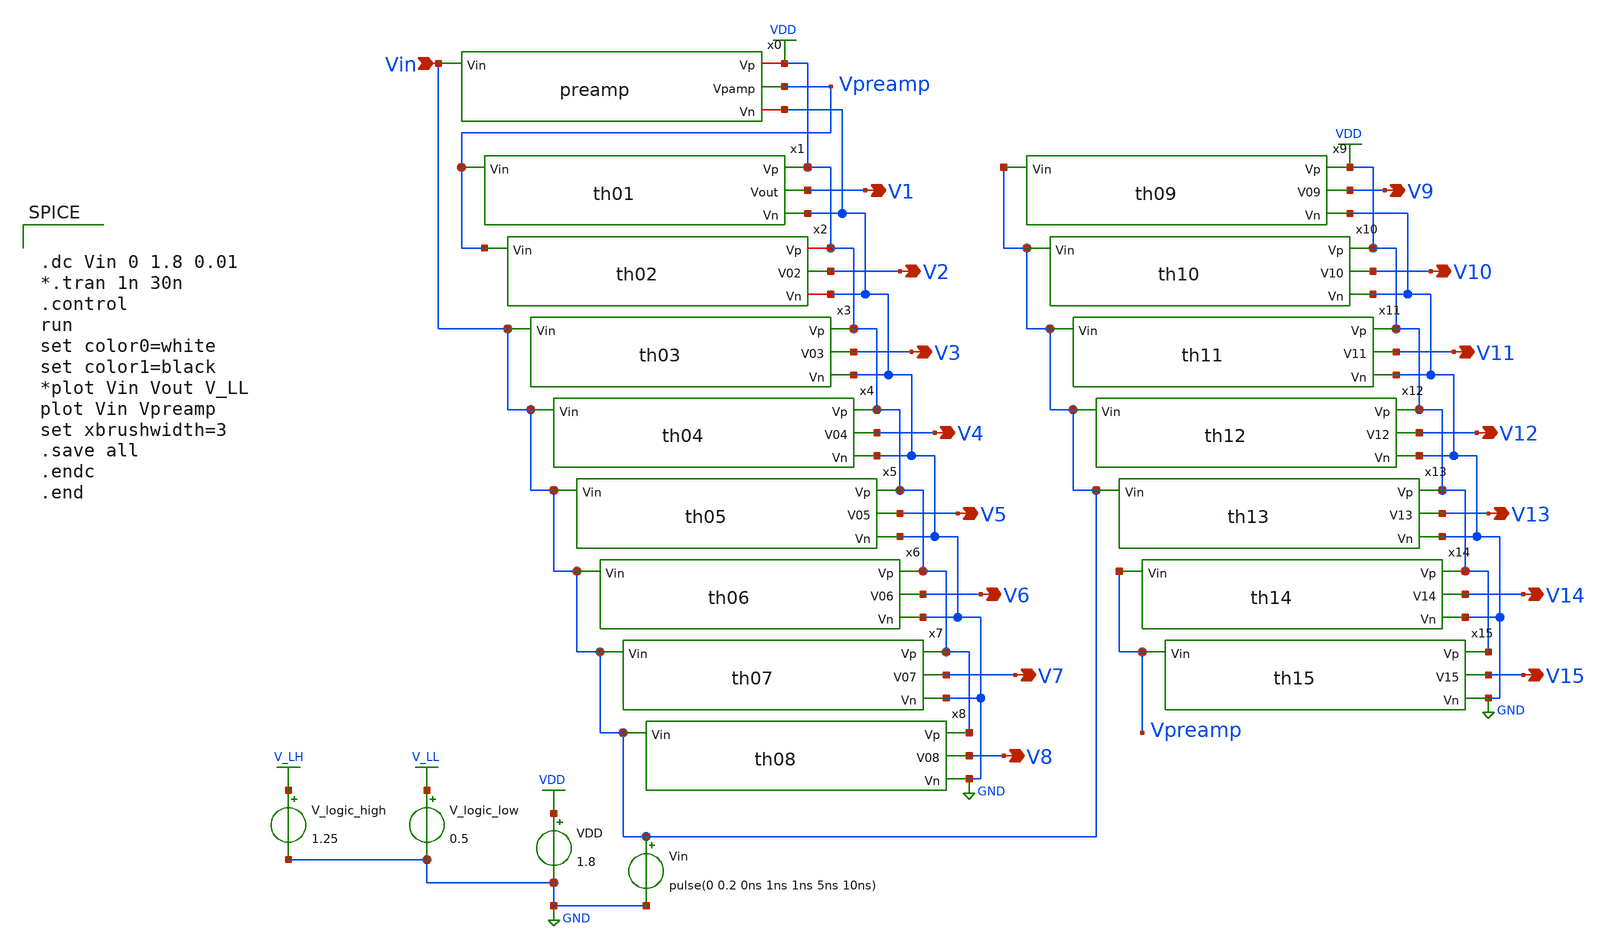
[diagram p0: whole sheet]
** sch_path: xschem/Vth_sch/Pre_layout/Analog_With_Sub.sch
**.subckt Analog_With_Sub V1 Vin V2 V3 V4 V5 V6 V7 V8 V9 V10 V11 V12 V13 V14 V15
*.opin V1
*.ipin Vin
*.opin V2
*.opin V3
*.opin V4
*.opin V5
*.opin V6
*.opin V7
*.opin V8
*.opin V9
*.opin V10
*.opin V11
*.opin V12
*.opin V13
*.opin V14
*.opin V15
VDD VDD GND 1.8
Vin Vin GND pulse(0 0.2 0ns 1ns 1ns 5ns 10ns)
V_logic_high V_LH GND 1.25
V_logic_low V_LL GND 0.5
x0 VDD Vin Vpreamp GND preamp
x1 VDD Vpreamp V1 GND th01
x2 VDD Vpreamp V2 GND th02
x3 VDD V3 Vin GND th03
x4 VDD V4 Vin GND th04
x5 VDD V5 Vin GND th05
x6 VDD Vin V6 GND th06
x7 VDD Vin V7 GND th07
x8 VDD V8 Vin GND th08
x9 VDD V9 Vin GND th09
x10 VDD V10 Vin GND th10
x11 VDD V11 Vin GND th11
x12 VDD V12 Vin GND th12
x13 VDD V13 Vin GND th13
x14 VDD V14 Vpreamp GND th14
x15 VDD V15 Vpreamp GND th15
**** begin user architecture code


.lib /usr/local/share/pdk/sky130A/libs.tech/ngspice/sky130.lib.spice tt

.save all





.dc Vin 0 1.8 0.01
*.tran 1n 30n
.control
run
set color0=white
set color1=black
*plot Vin Vout V_LL
plot Vin Vpreamp
set xbrushwidth=3
.save all
.endc
.end


**** end user architecture code
**.ends
.GLOBAL VDD
.GLOBAL GND
.GLOBAL V_LH
.GLOBAL V_LL
.end
